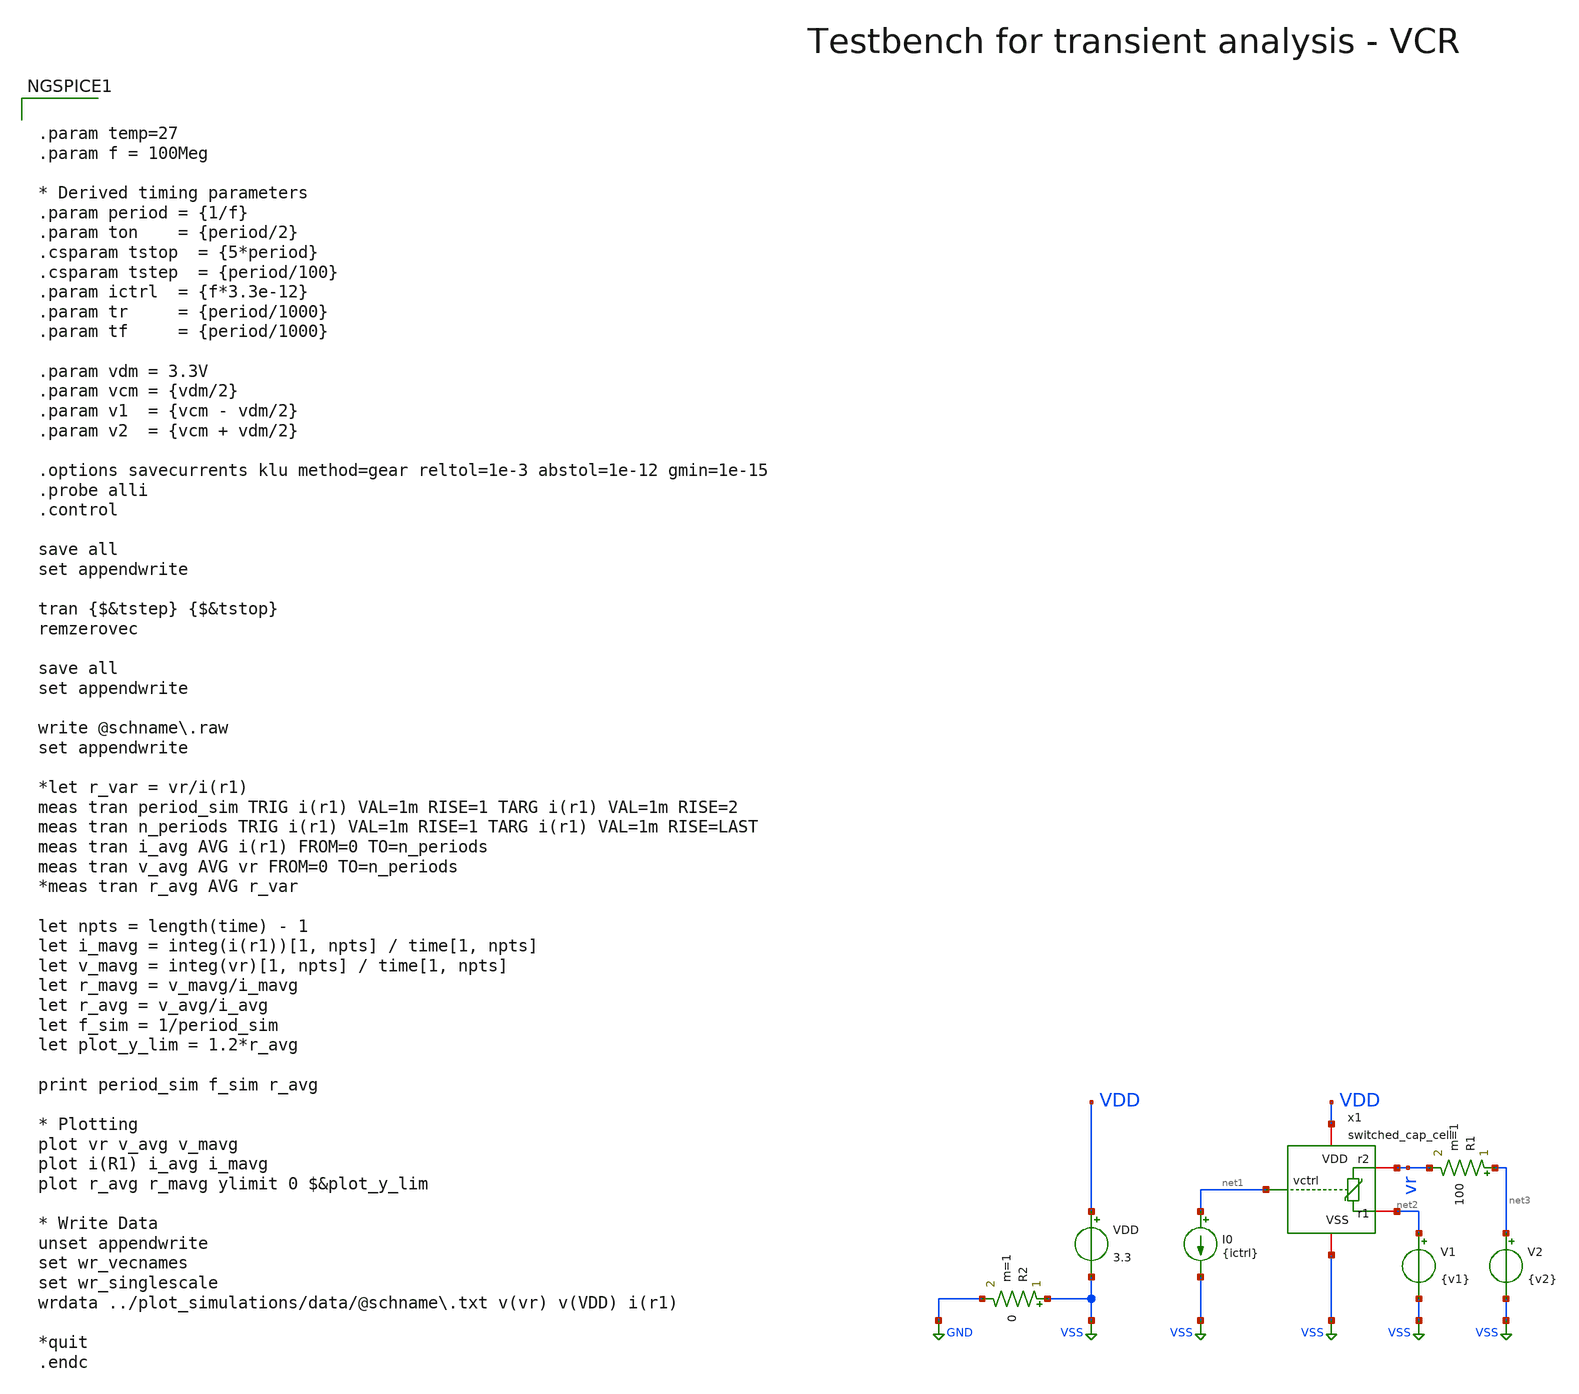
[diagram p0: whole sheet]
** sch_path: macros/heichips26_vcr/macros/switched_capacitor/testbenches/xschem/tb_switched_cap_tran.sch
**.subckt tb_switched_cap_tran
VDD VDD VSS 3.3
R2 VSS GND 0 m=1
I0 net1 VSS {ictrl}
R1 net3 vr 100 m=1
x1 net1 VDD VSS vr net2 switched_cap_cell
V1 net2 VSS {v1}
V2 net3 VSS {v2}
**** begin user architecture code

.lib cornerMOSlv.lib mos_tt
.lib cornerMOShv.lib mos_tt
.lib cornerRES.lib res_typ
.lib cornerDIO.lib dio_tt
.lib cornerCAP.lib cap_typ

.include $::PDK_ROOT/$::PDK/libs.ref/sg13cmos5l_stdcell/spice/sg13cmos5l_stdcell.spice



.param temp=27
.param f = 100Meg

* Derived timing parameters
.param period = {1/f}
.param ton    = {period/2}
.csparam tstop  = {5*period}
.csparam tstep  = {period/100}
.param ictrl  = {f*3.3e-12}
.param tr     = {period/1000}
.param tf     = {period/1000}

.param vdm = 3.3V
.param vcm = {vdm/2}
.param v1  = {vcm - vdm/2}
.param v2  = {vcm + vdm/2}

.options savecurrents klu method=gear reltol=1e-3 abstol=1e-12 gmin=1e-15
.probe alli
.control

save all
set appendwrite

tran {$&tstep} {$&tstop}
remzerovec

save all
set appendwrite

write @schname\.raw
set appendwrite

*let r_var = vr/i(r1)
meas tran period_sim TRIG i(r1) VAL=1m RISE=1 TARG i(r1) VAL=1m RISE=2
meas tran n_periods TRIG i(r1) VAL=1m RISE=1 TARG i(r1) VAL=1m RISE=LAST
meas tran i_avg AVG i(r1) FROM=0 TO=n_periods
meas tran v_avg AVG vr FROM=0 TO=n_periods
*meas tran r_avg AVG r_var

let npts = length(time) - 1
let i_mavg = integ(i(r1))[1, npts] / time[1, npts]
let v_mavg = integ(vr)[1, npts] / time[1, npts]
let r_mavg = v_mavg/i_mavg
let r_avg = v_avg/i_avg
let f_sim = 1/period_sim
let plot_y_lim = 1.2*r_avg

print period_sim f_sim r_avg

* Plotting
plot vr v_avg v_mavg
plot i(R1) i_avg i_mavg
plot r_avg r_mavg ylimit 0 $&plot_y_lim

* Write Data
unset appendwrite
set wr_vecnames
set wr_singlescale
wrdata ../plot_simulations/data/@schname\.txt v(vr) v(VDD) i(r1)

*quit
.endc


**** end user architecture code
**.ends

* expanding   symbol:  switched_cap_cell.sym # of pins=5
** sym_path: macros/heichips26_vcr/macros/switched_capacitor/schematic/xschem/switched_cap_cell.sym
** sch_path: macros/heichips26_vcr/macros/switched_capacitor/schematic/xschem/switched_cap_cell.sch
.subckt switched_cap_cell vctrl VDD VSS r2 r1
*.iopin r1
*.iopin r2
*.iopin VDD
*.iopin VSS
*.iopin vctrl
XC1 net2 VSS cap_cmomi w=30e-6 l=30e-6 mmin=1 mmax=4 feed=double subblock=0 m=1 mm_ok=1
XM2 net1 out1 VSS VSS sg13_hv_nmos w={n_w} l={n_l} ng={ng} m=1 mm_ok=1
XM3 net1 out1 VDD VDD sg13_hv_pmos w={p_w} l={p_l} ng={ng} m=1 mm_ok=1
x2 net6 net2 r1 net5 VDD VSS transmission_gate
x4 VDD net7 net4 VSS hv_inverter_40u
x5 VDD out1 vctrl VSS net9 net10 osc
x6 net8 net2 r2 net4 VDD VSS transmission_gate
x7 VDD net1 net7 VSS low_th_inverter
x8 VDD net1 net3 VSS high_th_inverter
x9 VDD net3 net6 VSS hv_inverter_40u
x10 VDD net6 net5 VSS hv_inverter_40u
x11 VDD net4 net8 VSS hv_inverter_40u
**** begin user architecture code


.param w   = 0.3u
.param ng  = 1
.param n_ng = ng
.param n_w = {w*n_ng}
.param n_l = 0.45u
.param p_ng = ng
.param p_w = {1*w*p_ng}
.param p_l = 0.4u


**** end user architecture code
.ends


* expanding   symbol:  transmission_gate.sym # of pins=6
** sym_path: macros/heichips26_vcr/macros/switched_capacitor/schematic/xschem/transmission_gate.sym
** sch_path: macros/heichips26_vcr/macros/switched_capacitor/schematic/xschem/transmission_gate.sch
.subckt transmission_gate vctrl vin vout nvctrl VDD VSS
*.iopin vin
*.iopin vout
*.ipin vctrl
*.ipin nvctrl
*.iopin VDD
*.iopin VSS
XM3 vout vctrl vin VSS sg13_hv_nmos w={tg_ngate_w*tg_ng} l={tg_ch_len} ng={tg_ng} m=1 mm_ok=1
XM4 vout nvctrl vin VDD sg13_hv_pmos w={tg_pgate_w*tg_ng} l={tg_ch_len} ng={tg_ng} m=1 mm_ok=1
**** begin user architecture code


.param tg_ch_len=1u
.param tg_ngate_w=2u
.param tg_pgate_w=10u
.param tg_ng=20


**** end user architecture code
.ends


* expanding   symbol:  hv_inverter_40u.sym # of pins=4
** sym_path: macros/heichips26_vcr/macros/switched_capacitor/schematic/xschem/hv_inverter_40u.sym
** sch_path: macros/heichips26_vcr/macros/switched_capacitor/schematic/xschem/hv_inverter_40u.sch
.subckt hv_inverter_40u VDD in out VSS
*.ipin in
*.iopin VDD
*.iopin VSS
*.opin out
XM2 out in VSS VSS sg13_hv_nmos w={n_w} l={n_l} ng={ng} m=1 mm_ok=1
XM3 out in VDD VDD sg13_hv_pmos w={p_w} l={p_l} ng={ng} m=1 mm_ok=1
**** begin user architecture code


.param w   = 10u
.param ng  = 4
.param n_ng = ng
.param n_w = {3u*n_ng}
.param n_l = 0.45u
.param p_ng = ng
.param p_w = {10u*p_ng}
.param p_l = 0.4u


**** end user architecture code
.ends


* expanding   symbol:  osc.sym # of pins=6
** sym_path: macros/heichips26_vcr/macros/switched_capacitor/schematic/xschem/osc.sym
** sch_path: macros/heichips26_vcr/macros/switched_capacitor/schematic/xschem/osc.sch
.subckt osc VDD out1 ictrl VSS start out2
*.iopin VSS
*.iopin VDD
*.iopin out2
*.iopin out1
*.iopin start
*.iopin ictrl
XM3 out1 ictrl VDD VDD sg13_hv_pmos w=10.0u l=2.0u ng=1 m=1 mm_ok=1
XM2 net1 ictrl VDD VDD sg13_hv_pmos w=1u l=2.0u ng=1 m=1 mm_ok=1
XM4 start ictrl VDD VDD sg13_hv_pmos w=1.0u l=2.0u ng=1 m=1 mm_ok=1
XM5 out2 ictrl VDD VDD sg13_hv_pmos w=10.0u l=2.0u ng=1 m=1 mm_ok=1
XM6 ictrl ictrl VDD VDD sg13_hv_pmos w=10.0u l=2.0u ng=1 m=1 mm_ok=1
XC1 net1 out1 cap_cmomi w=10e-6 l=10e-6 mmin=1 mmax=4 feed=double subblock=0 m=1 mm_ok=1
XC2 out2 start cap_cmomi w=10e-6 l=10e-6 mmin=1 mmax=4 feed=double subblock=0 m=1 mm_ok=1
XM8 out1 start VSS VSS sg13_hv_nmos w=3u l=0.45u ng=1 m=1 mm_ok=1
XM1 start start VSS VSS sg13_hv_nmos w=1u l=2u ng=1 m=1 mm_ok=1
XM12 out2 net1 VSS VSS sg13_hv_nmos w=3u l=0.45u ng=1 m=1 mm_ok=1
XM11 net1 net1 VSS VSS sg13_hv_nmos w=1u l=2u ng=1 m=1 mm_ok=1
**** begin user architecture code


.ic v(out1)=0 v(out2)=3.3


**** end user architecture code
.ends


* expanding   symbol:  low_th_inverter.sym # of pins=4
** sym_path: macros/heichips26_vcr/macros/switched_capacitor/schematic/xschem/low_th_inverter.sym
** sch_path: macros/heichips26_vcr/macros/switched_capacitor/schematic/xschem/low_th_inverter.sch
.subckt low_th_inverter VDD vin vout VSS
*.ipin vin
*.iopin VDD
*.iopin VSS
*.opin vout
XM1 vout vin VSS VSS sg13_hv_nmos w={n_ng*n_w} l={n_l} ng={n_ng} m=1 mm_ok=1
XM2 vout vin VDD VDD sg13_hv_pmos w={p_ng*p_w} l={p_l} ng={n_ng} m=1 mm_ok=1
**** begin user architecture code


.param n_ng = 2
.param n_w = 1u
.param n_l = 0.45u
.param p_ng = 2
.param p_w = 1u
.param p_l = 0.4u


**** end user architecture code
.ends


* expanding   symbol:  high_th_inverter.sym # of pins=4
** sym_path: macros/heichips26_vcr/macros/switched_capacitor/schematic/xschem/high_th_inverter.sym
** sch_path: macros/heichips26_vcr/macros/switched_capacitor/schematic/xschem/high_th_inverter.sch
.subckt high_th_inverter VDD vin vout VSS
*.ipin vin
*.iopin VDD
*.iopin VSS
*.opin vout
XMdummy1 VSS VSS VSS VSS sg13_hv_nmos w=0.6u l=1.0u ng=2 m=1 mm_ok=1
XMdummy2 VDD VDD VDD VDD sg13_hv_pmos w=12.0u l=1.0u ng=2 m=1 mm_ok=1
XM1 vout vin VSS VSS sg13_hv_nmos w=6.0u l=1.0u ng=20 m=1 mm_ok=1
XM2 vout vin VDD VDD sg13_hv_pmos w=120.0u l=1.0u ng=20 m=1 mm_ok=1
.ends

.GLOBAL VSS
.GLOBAL GND
.end
